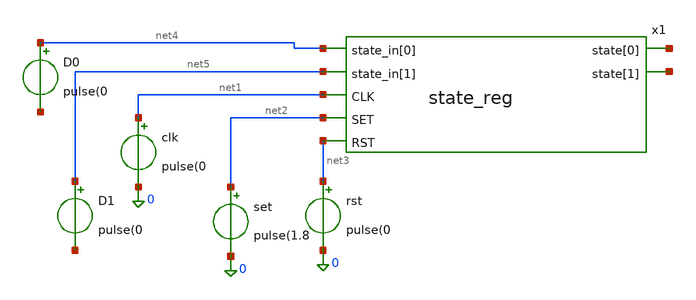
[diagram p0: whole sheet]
** sch_path: XSCHEM/reg_tb.sch
**.subckt reg_tb
clk net1 0 pulse(0
rst net3 0 pulse(0
set net2 0 pulse(1.8
D0 net4 net6 pulse(0
D1 net5 net7 pulse(0
x1 net8 net4 net5 net9 net1 net2 net3 state_reg
**** begin user architecture code

blab

**** end user architecture code
**.ends

* expanding   symbol:  /workspace/XSCHEM/state_reg.sym # of pins=7
** sym_path: XSCHEM/state_reg.sym
** sch_path: XSCHEM/state_reg.sch
.subckt state_reg state[0] state_in[0] state_in[1] state[1] CLK SET RST
*.ipin state_in[0]
*.ipin state_in[1]
*.ipin CLK
*.ipin SET
*.ipin RST
*.opin state[0]
*.opin state[1]
x1 CLK state_in[0] RST SET VGND VNB VPB VPWR state[0] net1 sky130_fd_sc_hd__dfbbp_1
x2 CLK state_in[1] RST SET VGND VNB VPB VPWR state[1] net2 sky130_fd_sc_hd__dfbbp_1
.ends

.end
